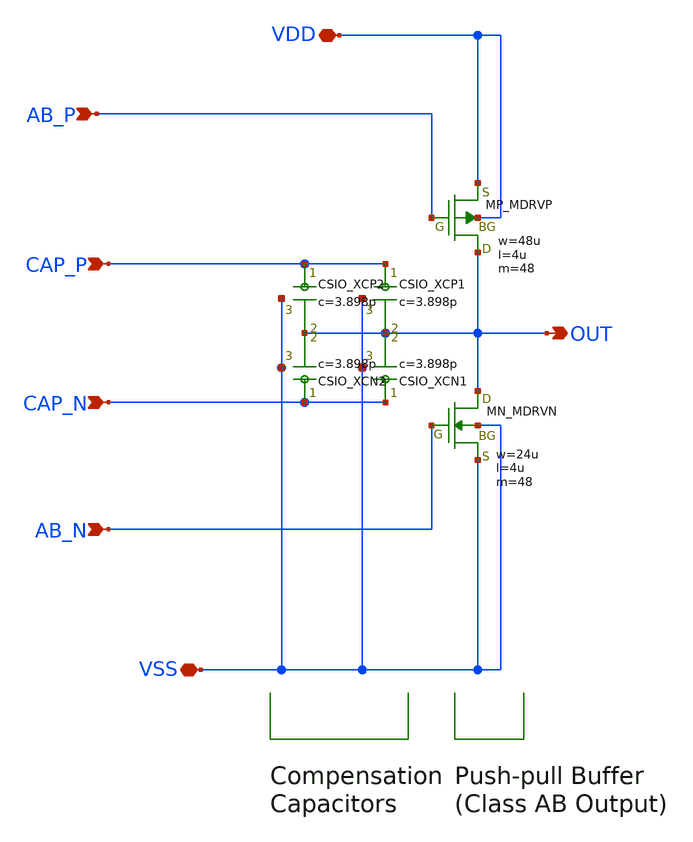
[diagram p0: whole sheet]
** sch_path: assets/images/handson/kyoto-ths/KM/opamp_r2r_ABAMP.sch
**.subckt opamp_r2r_ABAMP VDD VSS OUT AB_P AB_N CAP_P CAP_N
*.iopin VDD
*.iopin VSS
*.opin OUT
*.ipin AB_P
*.ipin AB_N
*.ipin CAP_P
*.ipin CAP_N
XMDRVP OUT AB_P VDD VDD PMOS w=48u l=4u as=0 ad=0 ps=0 pd=0 nrd=0 nrs=0 m=48
XMDRVN OUT AB_N VSS VSS NMOS w=24u l=4u as=0 ad=0 ps=0 pd=0 nrd=0 nrs=0 m=48
XXCP2 CAP_P OUT VSS F_CSIO c=3.898p x=80.6u y=80.6u m=1
XXCP1 CAP_P OUT VSS F_CSIO c=3.898p x=80.6u y=80.6u m=1
XXCN2 CAP_N OUT VSS F_CSIO c=3.898p x=80.6u y=80.6u m=1
XXCN1 CAP_N OUT VSS F_CSIO c=3.898p x=80.6u y=80.6u m=1
**.ends
.end
